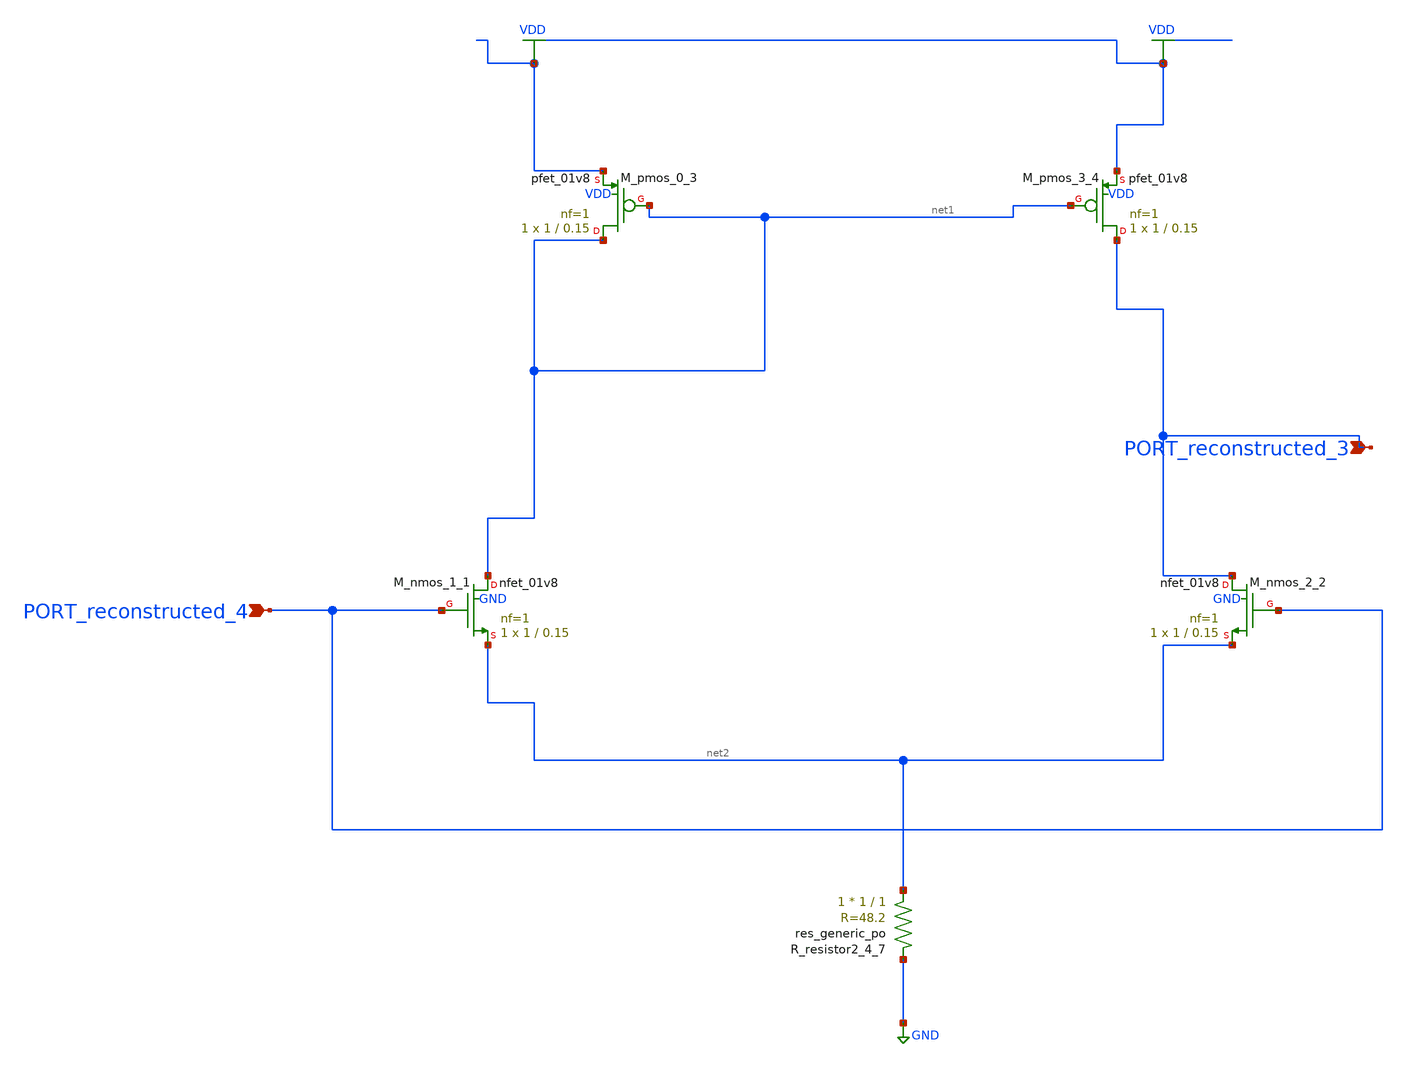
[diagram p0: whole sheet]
** sch_path: schematics/AMSNet/287.sch
**.subckt 287 PORT_reconstructed_3 PORT_reconstructed_4
*.ipin PORT_reconstructed_3
*.ipin PORT_reconstructed_4
XM_nmos_1_1 net1 PORT_reconstructed_4 net2 GND sky130_fd_pr__nfet_01v8 L=0.15 W=1 nf=1 ad='int((1 + 1)/2) * 1 / 1 * 0.29'
+ as='int((1 + 2)/2) * 1 / 1 * 0.29' pd='2*int((1 + 1)/2) * (1 / 1 + 0.29)' ps='2*int((1 + 2)/2) * (1 / 1 + 0.29)'
+ nrd='0.29 / 1 ' nrs='0.29 / 1 ' sa=0 sb=0 sd=0 mult=1 m=1
XM_nmos_2_2 PORT_reconstructed_3 PORT_reconstructed_4 net2 GND sky130_fd_pr__nfet_01v8 L=0.15 W=1 nf=1
+ ad='int((1 + 1)/2) * 1 / 1 * 0.29' as='int((1 + 2)/2) * 1 / 1 * 0.29' pd='2*int((1 + 1)/2) * (1 / 1 + 0.29)'
+ ps='2*int((1 + 2)/2) * (1 / 1 + 0.29)' nrd='0.29 / 1 ' nrs='0.29 / 1 ' sa=0 sb=0 sd=0 mult=1 m=1
XM_pmos_0_3 net1 net1 VDD VDD sky130_fd_pr__pfet_01v8 L=0.15 W=1 nf=1 ad='int((1 + 1)/2) * 1 / 1 * 0.29'
+ as='int((1 + 2)/2) * 1 / 1 * 0.29' pd='2*int((1 + 1)/2) * (1 / 1 + 0.29)' ps='2*int((1 + 2)/2) * (1 / 1 + 0.29)'
+ nrd='0.29 / 1 ' nrs='0.29 / 1 ' sa=0 sb=0 sd=0 mult=1 m=1
XM_pmos_3_4 PORT_reconstructed_3 net1 VDD VDD sky130_fd_pr__pfet_01v8 L=0.15 W=1 nf=1 ad='int((1 + 1)/2) * 1 / 1 * 0.29'
+ as='int((1 + 2)/2) * 1 / 1 * 0.29' pd='2*int((1 + 1)/2) * (1 / 1 + 0.29)' ps='2*int((1 + 2)/2) * (1 / 1 + 0.29)'
+ nrd='0.29 / 1 ' nrs='0.29 / 1 ' sa=0 sb=0 sd=0 mult=1 m=1
XR_resistor2_4_7 net2 GND sky130_fd_pr__res_generic_po W=1 L=1 m=1
**.ends
.GLOBAL GND
.GLOBAL VDD
.end
